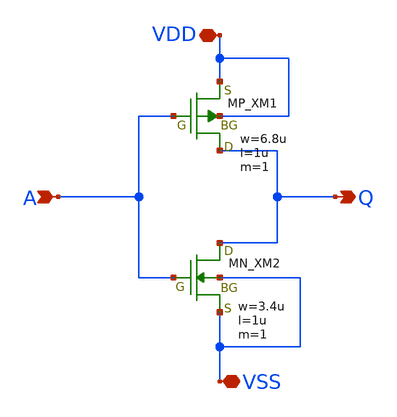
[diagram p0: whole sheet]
** sch_path: schematic/20250924_OSS_Workshop/Qdai/inverter_MUX_01/inv_hamasuna.sch
**.subckt inv_hamasuna VDD VSS A Q
*.iopin VDD
*.iopin VSS
*.ipin A
*.opin Q
XM1 Q A VDD VDD PMOS w=6.8u l=1u as=0 ad=0 ps=0 pd=0 nrd=0 nrs=0 m=1
XM2 Q A VSS VSS NMOS w=3.4u l=1u as=0 ad=0 ps=0 pd=0 nrd=0 nrs=0 m=1
**.ends
.end
